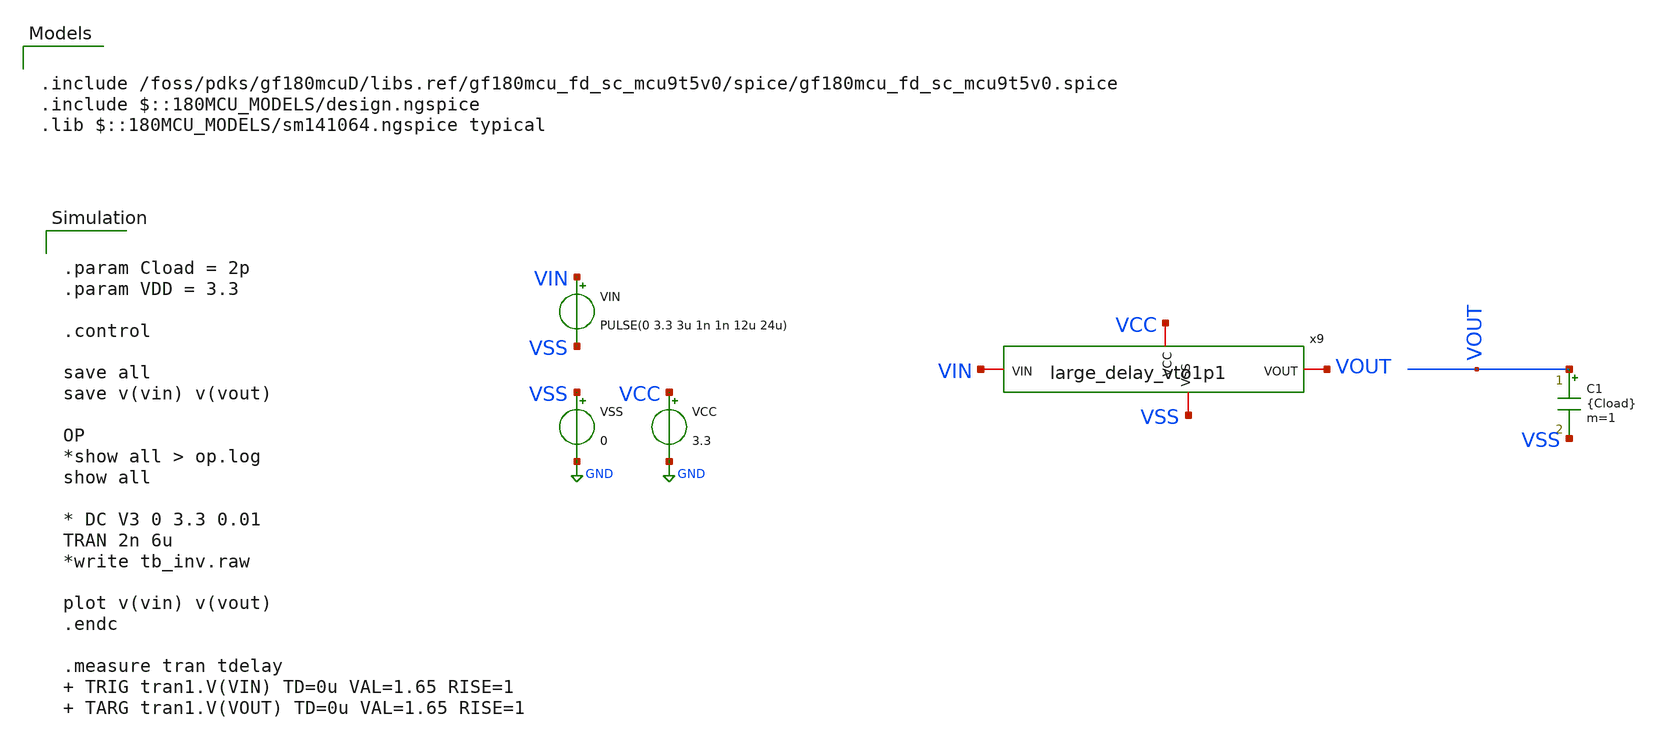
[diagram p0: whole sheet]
** sch_path: xschem/large_delay/tb_large_delay_vto1p1.sch
**.subckt tb_large_delay_vto1p1
VCC VCC GND 3.3
VSS VSS GND 0
VIN VIN VSS PULSE(0 3.3 3u 1n 1n 12u 24u)
C1 VOUT VSS {Cload} m=1
x9 VCC VSS VIN VOUT large_delay_vto1p1
**** begin user architecture code


.param Cload = 2p
.param VDD = 3.3

.control

save all
save v(vin) v(vout)

OP
*show all > op.log
show all

* DC V3 0 3.3 0.01
TRAN 2n 6u
*write tb_inv.raw

plot v(vin) v(vout)
.endc

.measure tran tdelay  TRIG tran1.V(VIN) TD=0u VAL=1.65 RISE=1  TARG tran1.V(VOUT) TD=0u VAL=1.65
+ RISE=1



.include /foss/pdks/gf180mcuD/libs.ref/gf180mcu_fd_sc_mcu9t5v0/spice/gf180mcu_fd_sc_mcu9t5v0.spice
.include $::180MCU_MODELS/design.ngspice
.lib $::180MCU_MODELS/sm141064.ngspice typical

**** end user architecture code
**.ends
.GLOBAL GND
.end
